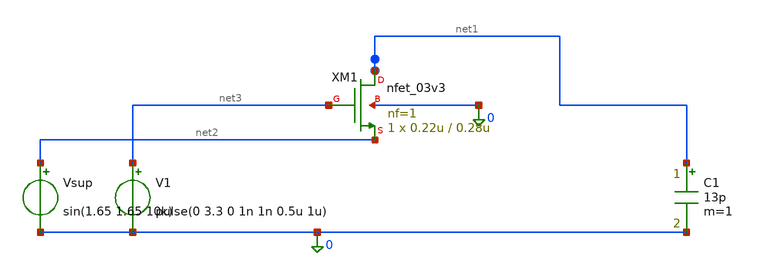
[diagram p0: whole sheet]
** sch_path: designs/emily_testing/TB_switch1.sch
**.subckt TB_switch1
V1 net3 0 pulse(0 3.3 0 1n 1n 0.5u 1u)
Vsup net2 0 sin(1.65 1.65 10k)
C1 net1 0 13p m=1
XM1 net1 net3 net2 0 nfet_03v3 L=0.28u W=0.22u nf=1 ad='int((nf+1)/2) * W/nf * 0.18u' as='int((nf+2)/2) * W/nf * 0.18u'
+ pd='2*int((nf+1)/2) * (W/nf + 0.18u)' ps='2*int((nf+2)/2) * (W/nf + 0.18u)' nrd='0.18u / W' nrs='0.18u / W'
+ sa=0 sb=0 sd=0 m=1
**** begin user architecture code


.lib /foss/pdks/gf180mcuD/libs.tech/ngspice/sm141064.ngspice nfet_03v3_t
.lib /foss/pdks/gf180mcuD/libs.tech/ngspice/sm141064.ngspice fets_mm
.include /foss/pdks/gf180mcuD/libs.tech/ngspice/design.ngspice
.param var_vth=0 var_k=0
.options savecurrents
.control
  save all
  tran 2n 3u
  let clk = v(net3)
  let vin = v(net2)
  let vout = v(net1)
  plot clk vin vout
.endc


**** end user architecture code
**.ends
.end
